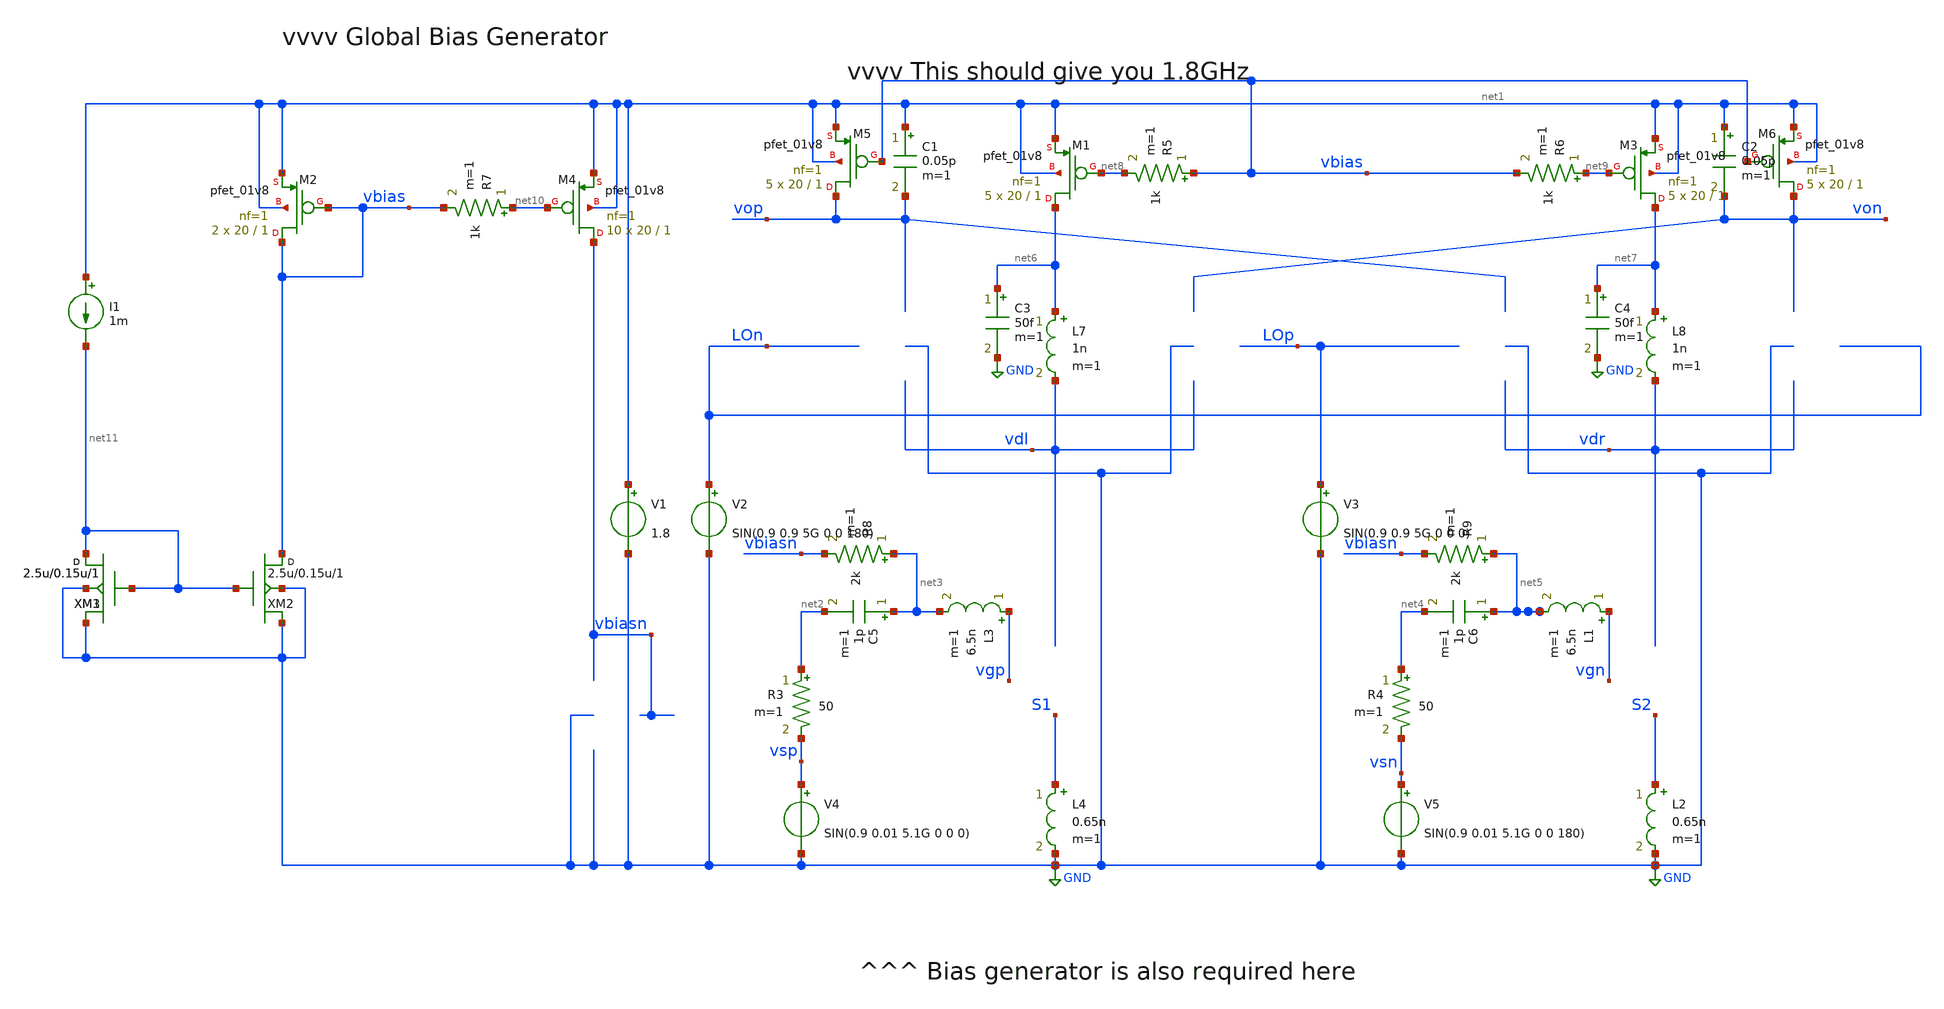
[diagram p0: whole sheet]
** sch_path: xschem/MIXER_5G_PEX.sch
**.subckt MIXER_5G_PEX
C1 net1 vop 0.05p m=1
C2 net1 von 0.05p m=1
V1 net1 GND 1.8
V2 LOn GND SIN(0.9 0.9 5G 0 0 180)
V3 LOp GND SIN(0.9 0.9 5G 0 0 0)
V4 vsp GND SIN(0.9 0.01 5.1G 0 0 0)
V5 vsn GND SIN(0.9 0.01 5.1G 0 0 180)
L3 vgp net3 6.5n m=1
L1 vgn net5 6.5n m=1
L2 S2 GND 0.65n m=1
L4 S1 GND 0.65n m=1
R3 net2 vsp 50 m=1
R4 net4 vsn 50 m=1
L7 net6 vdl 1n m=1
C3 net6 GND 50f m=1
L8 net7 vdr 1n m=1
C4 net7 GND 50f m=1
XM2 vbias vbias net1 net1 sky130_fd_pr__pfet_01v8 L=1 W=20 nf=1 ad='int((nf+1)/2) * W/nf * 0.29' as='int((nf+2)/2) * W/nf * 0.29'
+ pd='2*int((nf+1)/2) * (W/nf + 0.29)' ps='2*int((nf+2)/2) * (W/nf + 0.29)' nrd='0.29 / W' nrs='0.29 / W'
+ sa=0 sb=0 sd=0 mult=2 m=2
XM1 net6 net8 net1 net1 sky130_fd_pr__pfet_01v8 L=1 W=20 nf=1 ad='int((nf+1)/2) * W/nf * 0.29' as='int((nf+2)/2) * W/nf * 0.29'
+ pd='2*int((nf+1)/2) * (W/nf + 0.29)' ps='2*int((nf+2)/2) * (W/nf + 0.29)' nrd='0.29 / W' nrs='0.29 / W'
+ sa=0 sb=0 sd=0 mult=5 m=5
R5 vbias net8 1k m=1
XM3 net7 net9 net1 net1 sky130_fd_pr__pfet_01v8 L=1 W=20 nf=1 ad='int((nf+1)/2) * W/nf * 0.29' as='int((nf+2)/2) * W/nf * 0.29'
+ pd='2*int((nf+1)/2) * (W/nf + 0.29)' ps='2*int((nf+2)/2) * (W/nf + 0.29)' nrd='0.29 / W' nrs='0.29 / W'
+ sa=0 sb=0 sd=0 mult=5 m=5
R6 net9 vbias 1k m=1
XM4 vbiasn net10 net1 net1 sky130_fd_pr__pfet_01v8 L=1 W=20 nf=1 ad='int((nf+1)/2) * W/nf * 0.29' as='int((nf+2)/2) * W/nf * 0.29'
+ pd='2*int((nf+1)/2) * (W/nf + 0.29)' ps='2*int((nf+2)/2) * (W/nf + 0.29)' nrd='0.29 / W' nrs='0.29 / W'
+ sa=0 sb=0 sd=0 mult=10 m=10
R7 net10 vbias 1k m=1
C5 net3 net2 1p m=1
R8 net3 vbiasn 2k m=1
C6 net5 net4 1p m=1
R9 net5 vbiasn 2k m=1
XM5 vop vbias net1 net1 sky130_fd_pr__pfet_01v8 L=1 W=20 nf=1 ad='int((nf+1)/2) * W/nf * 0.29' as='int((nf+2)/2) * W/nf * 0.29'
+ pd='2*int((nf+1)/2) * (W/nf + 0.29)' ps='2*int((nf+2)/2) * (W/nf + 0.29)' nrd='0.29 / W' nrs='0.29 / W'
+ sa=0 sb=0 sd=0 mult=5 m=5
XM6 von vbias net1 net1 sky130_fd_pr__pfet_01v8 L=1 W=20 nf=1 ad='int((nf+1)/2) * W/nf * 0.29' as='int((nf+2)/2) * W/nf * 0.29'
+ pd='2*int((nf+1)/2) * (W/nf + 0.29)' ps='2*int((nf+2)/2) * (W/nf + 0.29)' nrd='0.29 / W' nrs='0.29 / W'
+ sa=0 sb=0 sd=0 mult=5 m=5
I1 net1 net11 1m
XM1 net11 net11 GND GND sky130_fd_pr__rf_nfet_01v8_bM04W5p00L0p15_ext w=2.5u l=0.15u m=1
XM2 vbias net11 GND GND sky130_fd_pr__rf_nfet_01v8_bM04W5p00L0p15_ext w=2.5u l=0.15u m=1
XM3 net11 net11 GND GND sky130_fd_pr__rf_nfet_01v8_bM04W5p00L0p15_ext w=2.5u l=0.15u m=1
**** begin user architecture code

.subckt sky130_fd_pr__rf_nfet_01v8_bM04W5p00L0p15_ext DRAIN GATE SOURCE SUBSTRATE
X0 DRAIN GATE SOURCE SUBSTRATE sky130_fd_pr__nfet_01v8 ad=2.828e+12p pd=2.132e+07u as=4.242e+12p
+ ps=3.198e+07u w=5.05e+06u l=150000u
X1 SOURCE SUBSTRATE SUBSTRATE SUBSTRATE sky130_fd_pr__nfet_01v8 ad=0p pd=0u as=3.03e+12p
+ ps=2.14e+07u w=5.05e+06u l=150000u
X2 SOURCE GATE DRAIN SUBSTRATE sky130_fd_pr__nfet_01v8 ad=0p pd=0u as=0p ps=0u w=5.05e+06u l=150000u
X3 DRAIN GATE SOURCE SUBSTRATE sky130_fd_pr__nfet_01v8 ad=0p pd=0u as=0p ps=0u w=5.05e+06u l=150000u
X4 SUBSTRATE SUBSTRATE SOURCE SUBSTRATE sky130_fd_pr__nfet_01v8 ad=0p pd=0u as=0p ps=0u w=5.05e+06u
+ l=150000u
X5 SOURCE GATE DRAIN SUBSTRATE sky130_fd_pr__nfet_01v8 ad=0p pd=0u as=0p ps=0u w=5.05e+06u l=150000u
.ends

.subckt NFET_extract_1 SD1 SD2 G1 G2 SUB
X0 SD1 G2 SD2 SUB sky130_fd_pr__nfet_01v8 ad=0p pd=0u as=0p ps=0u w=5.05e+06u l=150000u
X1 SD1 G2 SD2 SUB sky130_fd_pr__nfet_01v8 ad=0p pd=0u as=0p ps=0u w=5.05e+06u l=150000u
X2 SD2 G2 SD1 SUB sky130_fd_pr__nfet_01v8 ad=0p pd=0u as=0p ps=0u w=5.05e+06u l=150000u
X3 SD2 G2 SD1 SUB sky130_fd_pr__nfet_01v8 ad=0p pd=0u as=0p ps=0u w=5.05e+06u l=150000u
X4 SD1 G2 SD2 SUB sky130_fd_pr__nfet_01v8 ad=0p pd=0u as=0p ps=0u w=5.05e+06u l=150000u
X5 SD1 G2 SD2 SUB sky130_fd_pr__nfet_01v8 ad=0p pd=0u as=0p ps=0u w=5.05e+06u l=150000u
X6 SD2 G2 SD1 SUB sky130_fd_pr__nfet_01v8 ad=0p pd=0u as=0p ps=0u w=5.05e+06u l=150000u
X7 SD2 G2 SD1 SUB sky130_fd_pr__nfet_01v8 ad=0p pd=0u as=0p ps=0u w=5.05e+06u l=150000u
X8 SD1 G2 SD2 SUB sky130_fd_pr__nfet_01v8 ad=0p pd=0u as=0p ps=0u w=5.05e+06u l=150000u
X9 SD1 G2 SD2 SUB sky130_fd_pr__nfet_01v8 ad=0p pd=0u as=0p ps=0u w=5.05e+06u l=150000u
X10 SD2 G2 SD1 SUB sky130_fd_pr__nfet_01v8 ad=0p pd=0u as=0p ps=0u w=5.05e+06u l=150000u
X11 SD2 G2 SD1 SUB sky130_fd_pr__nfet_01v8 ad=0p pd=0u as=0p ps=0u w=5.05e+06u l=150000u
C0 SUB SD1 3.04fF
C1 G2 SD2 3.72fF
C2 G2 SD1 4.78fF
C3 SD1 SD2 30.67fF
C4 G2 SUB 2.48fF
C5 G2 SUB 3.11fF
C6 SD1 SUB 6.93fF
.ends

* Input Transconductance
XMEXT_0_0 vdl S1 vgp vgp GND NFET_extract_1
XMEXT_0_1 vdl S1 vgp vgp GND NFET_extract_1
XMEXT_1_0 vdr S2 vgn vgn GND NFET_extract_1
XMEXT_1_1 vdr S2 vgn vgn GND NFET_extract_1

* Current Source

XMEXT_IREF_0 vbiasn GND vbiasn vbiasn GND NFET_extract_1
XMEXT_IREF_1 vbiasn GND vbiasn vbiasn GND NFET_extract_1


* Switches
XMEXT_l1_0 vop vdl LOn LOn GND NFET_extract_1
XMEXT_l2_0 von vdl LOp LOp GND NFET_extract_1
XMEXT_r1_0 vop vdr LOp LOp GND NFET_extract_1
XMEXT_r2_0 von vdr LOn LOn GND NFET_extract_1

XMEXT_l1_1 vop vdl LOn LOn GND NFET_extract_1
XMEXT_l2_1 von vdl LOp LOp GND NFET_extract_1
XMEXT_r1_1 vop vdr LOp LOp GND NFET_extract_1
XMEXT_r2_1 von vdr LOn LOn GND NFET_extract_1
.options savecurrents

.tran 10ps 50ns
.control
run
display
*let m_start = 9
*let m_stop  = 14
*let m_delta = 1
let vo = v(vop)-v(von)
let vs = v(vsp)-v(vsn)
let vg = v(vgp)-v(vgn)

*let m_var = m_start
*while m_var le m_stop
*  print m_var
*  alter @m.xm1.msky130_fd_pr__pfet_01v8[m] = m_var
*  alter @m.xm3.msky130_fd_pr__pfet_01v8[m] = m_var

*  tran 10ps 50ns
*  * plot v(von) v(vop)
*  let vo = v(vop)-v(von)
plot @l7[i]
plot vo
*  let m_var = m_var + m_delta
*end


* plot vo
plot vs
plot vg
* fft vo vs vg
* plot db(vo) db(vs)



.endc


.lib $::SKYWATER_MODELS/sky130.lib.spice tt
* .include $::PDKPATH/libs.ref/sky130_fd_sc_hvl/spice/sky130_fd_sc_hvl.spice

**** end user architecture code
**.ends
.GLOBAL GND
.end
